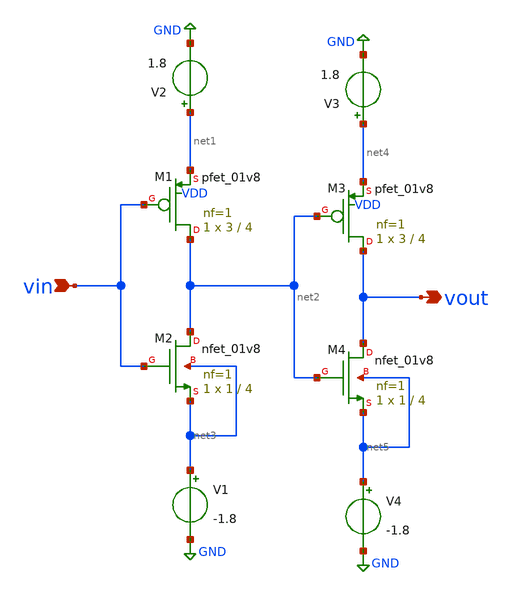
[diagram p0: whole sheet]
** sch_path: buffer_for_symbol.sch
**.subckt buffer_for_symbol vin vout
*.ipin vin
*.opin vout
XM1 net2 vin net1 VDD sky130_fd_pr__pfet_01v8 L=4 W=3 nf=1 ad='int((nf+1)/2) * W/nf * 0.29' as='int((nf+2)/2) * W/nf * 0.29'
+ pd='2*int((nf+1)/2) * (W/nf + 0.29)' ps='2*int((nf+2)/2) * (W/nf + 0.29)' nrd='0.29 / W' nrs='0.29 / W'
+ sa=0 sb=0 sd=0 mult=1 m=1
XM2 net2 vin net3 net3 sky130_fd_pr__nfet_01v8 L=4 W=1 nf=1 ad='int((nf+1)/2) * W/nf * 0.29' as='int((nf+2)/2) * W/nf * 0.29'
+ pd='2*int((nf+1)/2) * (W/nf + 0.29)' ps='2*int((nf+2)/2) * (W/nf + 0.29)' nrd='0.29 / W' nrs='0.29 / W'
+ sa=0 sb=0 sd=0 mult=1 m=1
V2 net1 GND 1.8
XM3 vout net2 net4 VDD sky130_fd_pr__pfet_01v8 L=4 W=3 nf=1 ad='int((nf+1)/2) * W/nf * 0.29' as='int((nf+2)/2) * W/nf * 0.29'
+ pd='2*int((nf+1)/2) * (W/nf + 0.29)' ps='2*int((nf+2)/2) * (W/nf + 0.29)' nrd='0.29 / W' nrs='0.29 / W'
+ sa=0 sb=0 sd=0 mult=1 m=1
XM4 vout net2 net5 net5 sky130_fd_pr__nfet_01v8 L=4 W=1 nf=1 ad='int((nf+1)/2) * W/nf * 0.29' as='int((nf+2)/2) * W/nf * 0.29'
+ pd='2*int((nf+1)/2) * (W/nf + 0.29)' ps='2*int((nf+2)/2) * (W/nf + 0.29)' nrd='0.29 / W' nrs='0.29 / W'
+ sa=0 sb=0 sd=0 mult=1 m=1
V3 net4 GND 1.8
V1 net3 GND -1.8
V4 net5 GND -1.8
**.ends
.GLOBAL GND
.end
